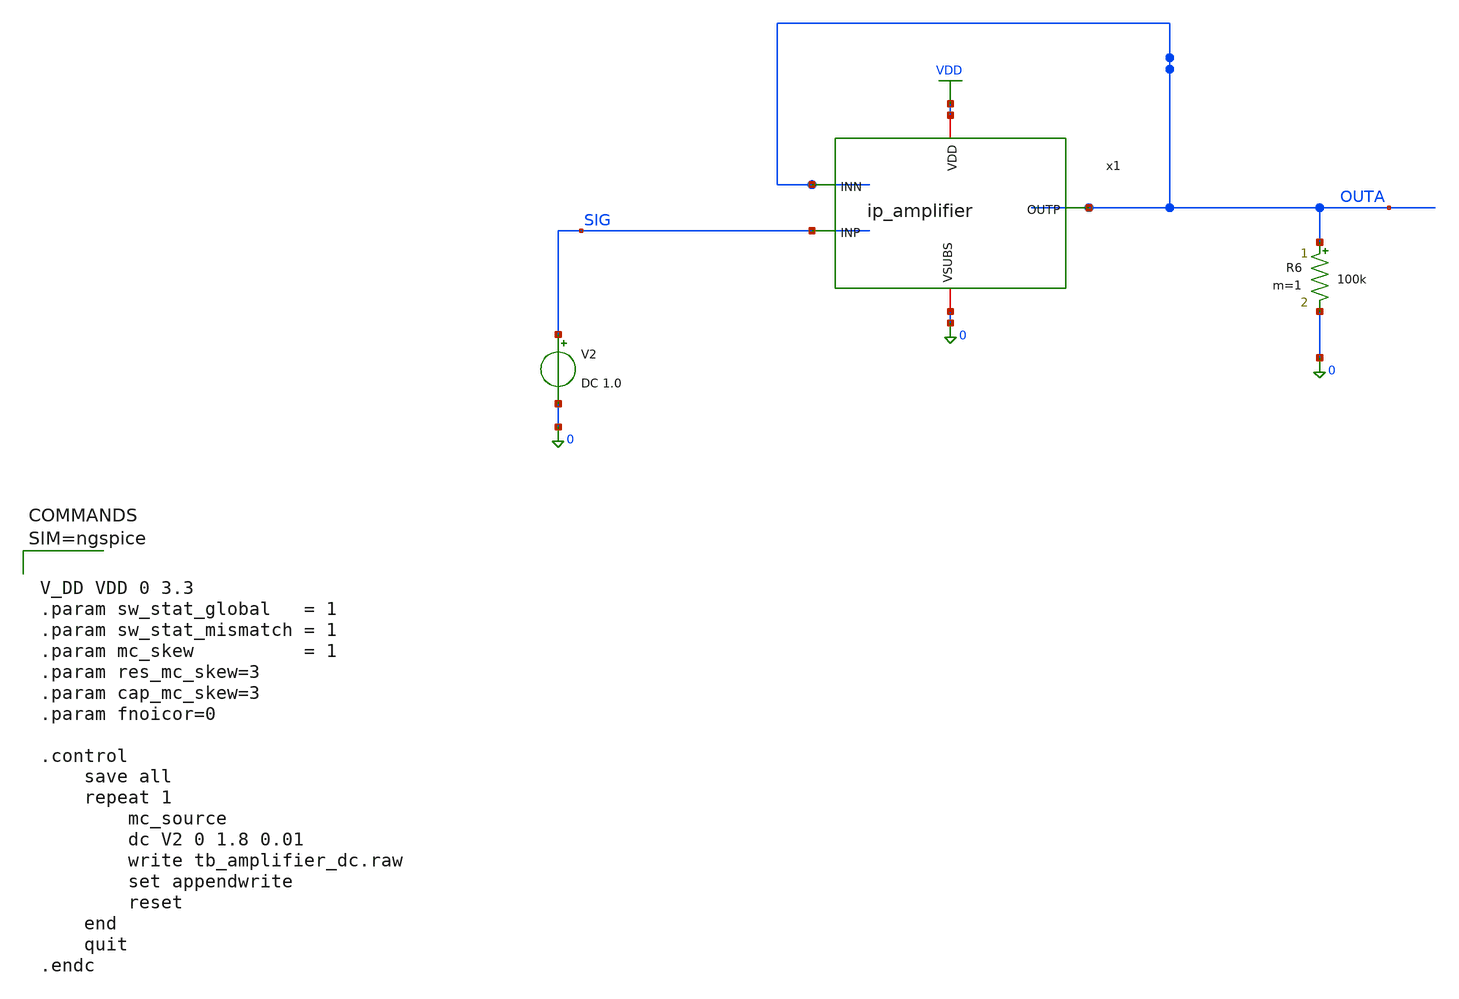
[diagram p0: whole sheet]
** sch_path: xschem/tb_amplifier_dc.sch
**.subckt tb_amplifier_dc
x1 VDD OUTA SIG OUTA 0 ip_amplifier
R6 OUTA 0 100k m=1
V2 SIG 0 DC 1.0
**** begin user architecture code

.lib $::180MCU_MODELS/sm141064.ngspice statistical
.lib $::180MCU_MODELS/sm141064.ngspice moscap_typical
.lib $::180MCU_MODELS/sm141064.ngspice diode_typical
.lib $::180MCU_MODELS/sm141064.ngspice res_statistical




V_DD VDD 0 3.3
.param sw_stat_global   = 1
.param sw_stat_mismatch = 1
.param mc_skew          = 1
.param res_mc_skew=3
.param cap_mc_skew=3
.param fnoicor=0

.control
	save all
	repeat 1
		mc_source
		dc V2 0 1.8 0.01
		write tb_amplifier_dc.raw
		set appendwrite
		reset
	end
	quit
.endc



**** end user architecture code
**.ends
.GLOBAL VDD
.end
